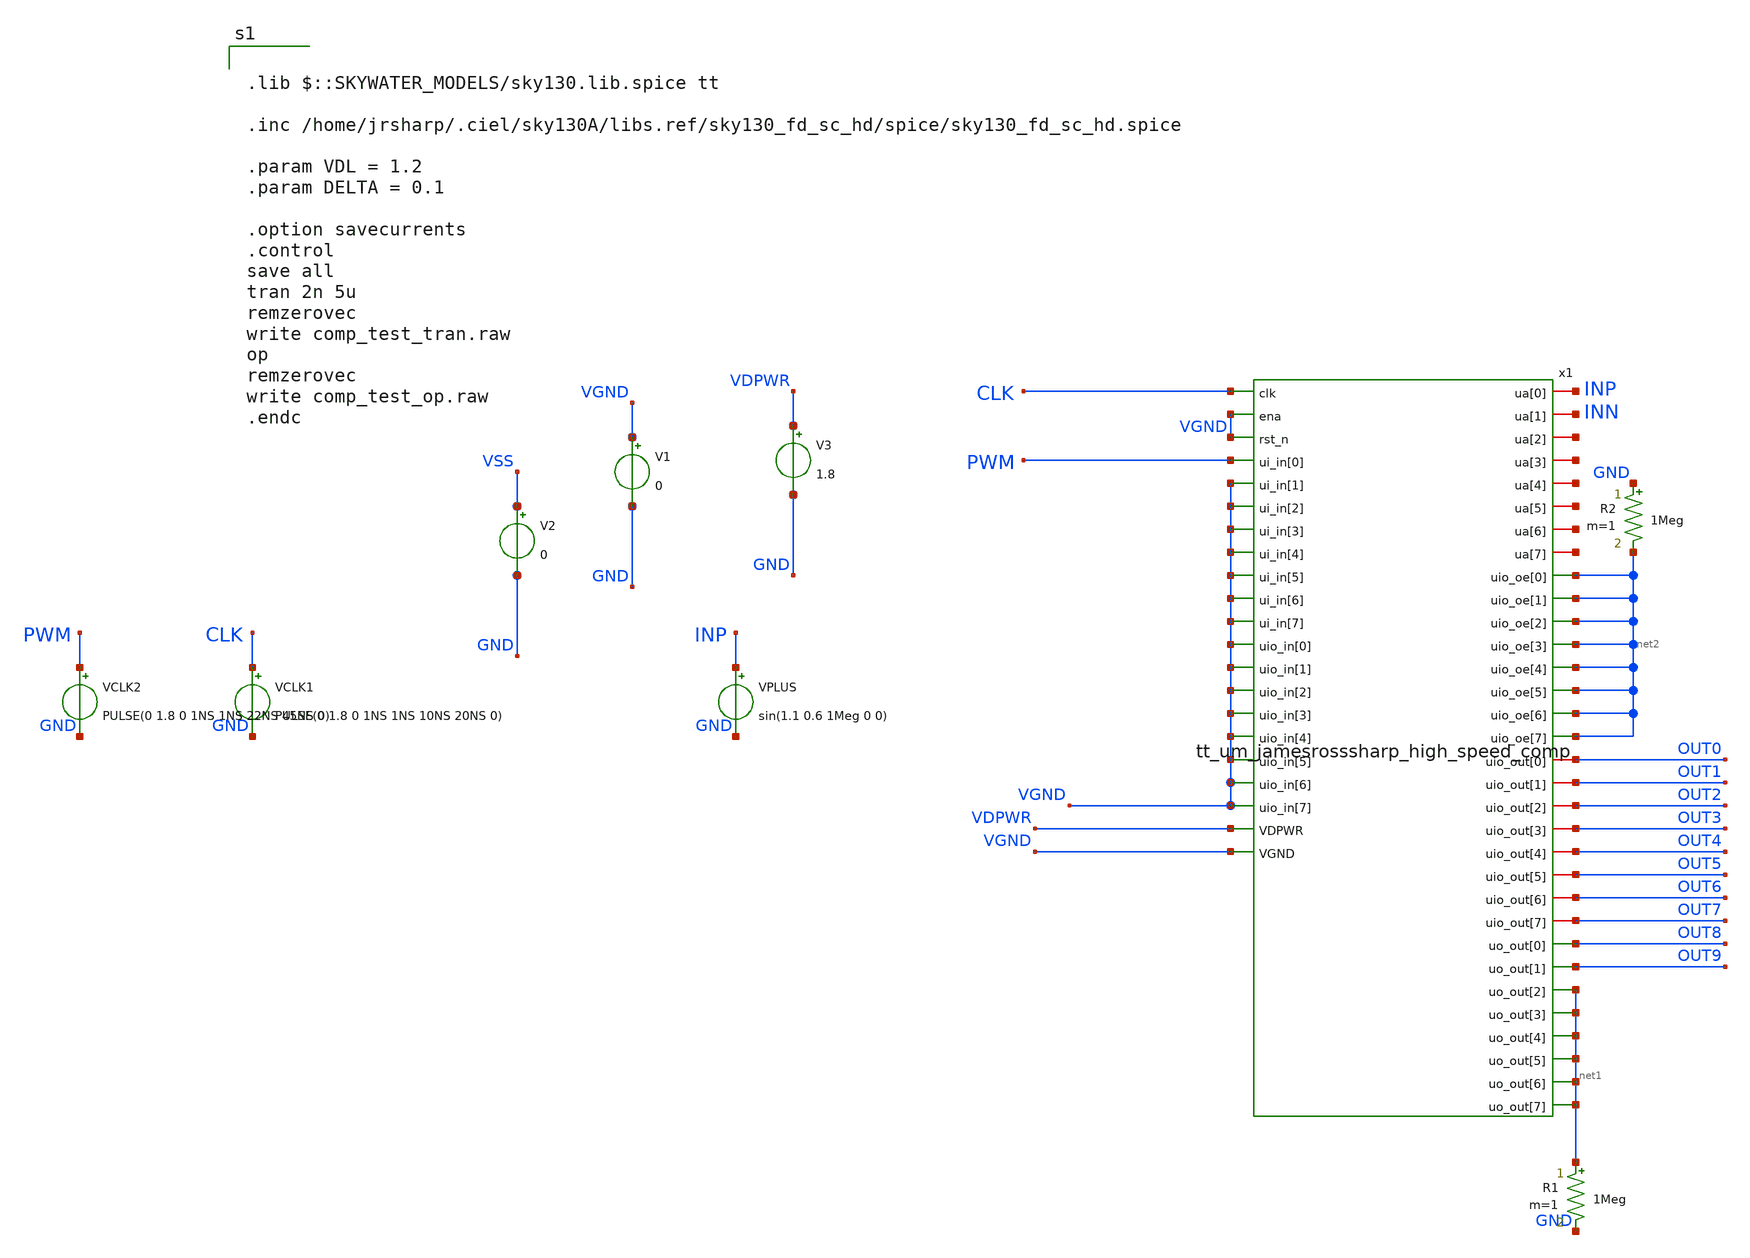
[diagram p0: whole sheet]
** sch_path: xschem/tt/tt_um_jamesrosssharp_high_speed_comp_test.sch
**.subckt tt_um_jamesrosssharp_high_speed_comp_test
x1 CLK VGND VGND PWM INP VGND INN VGND net3 VGND net4 VGND net5 VGND net6 VGND net7 VGND net8 VGND
+ VGND VGND VGND VGND VGND VGND VGND net2 net2 net2 net2 net2 net2 net2 net2 OUT0 OUT1 OUT2 OUT3 OUT4 OUT5
+ OUT6 OUT7 OUT8 OUT9 net1 net1 net1 net1 net1 net1 VDPWR VGND tt_um_jamesrosssharp_high_speed_comp
VPLUS INP GND sin(1.1 0.6 1Meg 0 0)
VCLK1 CLK GND PULSE(0 1.8 0 1NS 1NS 10NS 20NS 0)
V3 VDPWR GND 1.8
V1 VGND GND 0
R1 net1 GND 1Meg m=1
R2 GND net2 1Meg m=1
V2 VSS GND 0
VCLK2 PWM GND PULSE(0 1.8 0 1NS 1NS 22NS 45NS 0)
**** begin user architecture code

.lib $::SKYWATER_MODELS/sky130.lib.spice tt

.inc /home/jrsharp/.ciel/sky130A/libs.ref/sky130_fd_sc_hd/spice/sky130_fd_sc_hd.spice

.param VDL = 1.2
.param DELTA = 0.1

.option savecurrents
.control
save all
tran 2n 5u
remzerovec
write comp_test_tran.raw
op
remzerovec
write comp_test_op.raw
.endc



**** end user architecture code
**.ends

* expanding   symbol:  tt_um_jamesrosssharp_high_speed_comp.sym # of pins=53
** sym_path: xschem/tt/tt_um_jamesrosssharp_high_speed_comp.sym
** sch_path: xschem/tt/tt_um_jamesrosssharp_high_speed_comp.sch
.subckt tt_um_jamesrosssharp_high_speed_comp clk ena rst_n ui_in[0] ua[0] ui_in[1] ua[1] ui_in[2]
+ ua[2] ui_in[3] ua[3] ui_in[4] ua[4] ui_in[5] ua[5] ui_in[6] ua[6] ui_in[7] ua[7] uio_in[0] uio_in[1]
+ uio_in[2] uio_in[3] uio_in[4] uio_in[5] uio_in[6] uio_in[7] uio_oe[0] uio_oe[1] uio_oe[2] uio_oe[3] uio_oe[4]
+ uio_oe[5] uio_oe[6] uio_oe[7] uio_out[0] uio_out[1] uio_out[2] uio_out[3] uio_out[4] uio_out[5] uio_out[6]
+ uio_out[7] uo_out[0] uo_out[1] uo_out[2] uo_out[3] uo_out[4] uo_out[5] uo_out[6] uo_out[7] VDPWR VGND
*.ipin clk
*.ipin ena
*.ipin rst_n
*.iopin ua[0]
*.iopin ua[1]
*.iopin ua[2]
*.iopin ua[3]
*.iopin ua[4]
*.iopin ua[5]
*.iopin ua[6]
*.iopin ua[7]
*.ipin ui_in[0]
*.ipin ui_in[1]
*.ipin ui_in[2]
*.ipin ui_in[3]
*.ipin ui_in[4]
*.ipin ui_in[5]
*.ipin ui_in[6]
*.ipin ui_in[7]
*.ipin uio_in[0]
*.ipin uio_in[1]
*.ipin uio_in[2]
*.ipin uio_in[3]
*.ipin uio_in[4]
*.ipin uio_in[5]
*.ipin uio_in[6]
*.ipin uio_in[7]
*.opin uio_oe[0]
*.opin uio_oe[1]
*.opin uio_oe[2]
*.opin uio_oe[3]
*.opin uio_oe[4]
*.opin uio_oe[5]
*.opin uio_oe[6]
*.opin uio_oe[7]
*.iopin uio_out[0]
*.iopin uio_out[1]
*.iopin uio_out[2]
*.iopin uio_out[3]
*.iopin uio_out[4]
*.iopin uio_out[5]
*.iopin uio_out[6]
*.iopin uio_out[7]
*.opin uo_out[0]
*.opin uo_out[1]
*.opin uo_out[2]
*.opin uo_out[3]
*.opin uo_out[4]
*.opin uo_out[5]
*.opin uo_out[6]
*.opin uo_out[7]
*.ipin VDPWR
*.ipin VGND
x1 ua[0] VDPWR VGND ui_in[0] clk_prime net1 ua[1] 1bit_am
x2 net6 clk_prime ua[0] net14 net7 VDPWR VGND net8 net9 net13 net12 net11 net10 net3 flash_converter
x3 VGND VNB VPB VPWR uio_oe[0] net15 sky130_fd_sc_hd__conb_1
x4 VGND VNB VPB VPWR uio_oe[1] net16 sky130_fd_sc_hd__conb_1
x5 VGND VNB VPB VPWR uio_oe[2] net17 sky130_fd_sc_hd__conb_1
x6 VGND VNB VPB VPWR uio_oe[3] net18 sky130_fd_sc_hd__conb_1
x7 VGND VNB VPB VPWR uio_oe[4] net19 sky130_fd_sc_hd__conb_1
x8 VGND VNB VPB VPWR uio_oe[5] net20 sky130_fd_sc_hd__conb_1
x9 VGND VNB VPB VPWR uio_oe[6] net21 sky130_fd_sc_hd__conb_1
x10 VGND VNB VPB VPWR uio_oe[7] net22 sky130_fd_sc_hd__conb_1
x11 clk_prime ua[0] ua[1] VDPWR net2 VGND high_speed_comp_top
x12 VGND VNB VPB VPWR net23 uo_out[2] sky130_fd_sc_hd__conb_1
x13 VGND VNB VPB VPWR net24 uo_out[3] sky130_fd_sc_hd__conb_1
x14 VGND VNB VPB VPWR net25 uo_out[4] sky130_fd_sc_hd__conb_1
x15 VGND VNB VPB VPWR net26 uo_out[5] sky130_fd_sc_hd__conb_1
x16 VGND VNB VPB VPWR net27 uo_out[6] sky130_fd_sc_hd__conb_1
x17 VGND VNB VPB VPWR net28 uo_out[7] sky130_fd_sc_hd__conb_1
XR11 net6 VDPWR VGND sky130_fd_pr__res_high_po_1p41 L=1.41 mult=1 m=1
XR1 net3 net4 VGND sky130_fd_pr__res_high_po_1p41 L=1.41 mult=1 m=1
XR2 net4 net5 VGND sky130_fd_pr__res_high_po_1p41 L=1.41 mult=1 m=1
XR3 net5 VGND VGND sky130_fd_pr__res_high_po_1p41 L=1.41 mult=1 m=1
x18 clk VGND VGND VDPWR VDPWR clk_prime sky130_fd_sc_hd__clkbuf_16
x19 VGND VGND VDPWR VDPWR sky130_fd_sc_hd__decap_3
x20 VGND VDPWR sky130_fd_sc_hd__tapvpwrvgnd_1
x21 net2 VGND VGND VDPWR VDPWR uo_out[1] sky130_fd_sc_hd__buf_16
x22 net1 VGND VGND VDPWR VDPWR uo_out[0] sky130_fd_sc_hd__buf_16
x23 VGND VGND VDPWR VDPWR sky130_fd_sc_hd__decap_3
x24 VGND VDPWR sky130_fd_sc_hd__tapvpwrvgnd_1
x25 VGND VGND VDPWR VDPWR sky130_fd_sc_hd__decap_3
x26 VGND VDPWR sky130_fd_sc_hd__tapvpwrvgnd_1
x27 net14 VGND VGND VDPWR VDPWR uio_out[0] sky130_fd_sc_hd__buf_16
x28 net7 VGND VGND VDPWR VDPWR uio_out[1] sky130_fd_sc_hd__buf_16
x29 net8 VGND VGND VDPWR VDPWR uio_out[2] sky130_fd_sc_hd__buf_16
x31 net13 VGND VGND VDPWR VDPWR uio_out[4] sky130_fd_sc_hd__buf_16
x32 net12 VGND VGND VDPWR VDPWR uio_out[5] sky130_fd_sc_hd__buf_16
x33 net11 VGND VGND VDPWR VDPWR uio_out[6] sky130_fd_sc_hd__buf_16
x34 net10 VGND VGND VDPWR VDPWR uio_out[7] sky130_fd_sc_hd__buf_16
x30 net9 VGND VGND VDPWR VDPWR uio_out[3] sky130_fd_sc_hd__buf_16
x35 VGND VGND VDPWR VDPWR sky130_fd_sc_hd__decap_3
x36 VGND VDPWR sky130_fd_sc_hd__tapvpwrvgnd_1
x37 VGND VGND VDPWR VDPWR sky130_fd_sc_hd__decap_3
x38 VGND VDPWR sky130_fd_sc_hd__tapvpwrvgnd_1
x39 VGND VGND VDPWR VDPWR sky130_fd_sc_hd__decap_3
x40 VGND VDPWR sky130_fd_sc_hd__tapvpwrvgnd_1
.ends


* expanding   symbol:  1bit_am.sym # of pins=7
** sym_path: xschem/1bit_am/1bit_am.sym
** sch_path: xschem/1bit_am/1bit_am.sch
.subckt 1bit_am VIN VDD VSS PWM_IN CLK VOUT VIN_MINUS
*.ipin VDD
*.ipin VSS
*.ipin CLK
*.ipin VIN
*.opin VOUT
*.ipin PWM_IN
*.ipin VIN_MINUS
x1 CLK NET_IN VIN_MINUS VDD VOUT VSS high_speed_comp_top
XR2 net2 VIN_MINUS VSS sky130_fd_pr__res_xhigh_po_0p35 L=30 mult=1 m=1
XR3 VDD net3 VSS sky130_fd_pr__res_xhigh_po_0p35 L=20 mult=1 m=1
XR4 net3 NET_IN VSS sky130_fd_pr__res_xhigh_po_0p35 L=20 mult=1 m=1
XR5 NET_IN net4 VSS sky130_fd_pr__res_xhigh_po_0p35 L=20 mult=1 m=1
XR6 net4 VSS VSS sky130_fd_pr__res_xhigh_po_0p35 L=20 mult=1 m=1
XC1 VIN NET_IN sky130_fd_pr__cap_mim_m3_1 W=10 L=10 MF=20 m=20
XC2 VIN_MINUS VSS sky130_fd_pr__cap_mim_m3_1 W=10 L=10 MF=20 m=20
x4 VSS VSS VDD VDD sky130_fd_sc_hd__decap_3
x5 VSS VSS VDD VDD sky130_fd_sc_hd__decap_3
x6 VSS VDD sky130_fd_sc_hd__tapvpwrvgnd_1
x7 VSS VDD sky130_fd_sc_hd__tapvpwrvgnd_1
XR1 net5 net6 VSS sky130_fd_pr__res_xhigh_po_0p35 L=30 mult=1 m=1
x3 PWM_IN VSS VSS VDD VDD net1 sky130_fd_sc_hd__inv_1
XR7 net6 net7 VSS sky130_fd_pr__res_xhigh_po_0p35 L=30 mult=1 m=1
XR8 net7 net2 VSS sky130_fd_pr__res_xhigh_po_0p35 L=30 mult=1 m=1
x2 net1 VSS VSS VDD VDD net5 sky130_fd_sc_hd__inv_1
.ends


* expanding   symbol:  flash_converter.sym # of pins=14
** sym_path: xschem/flash_converter/flash_converter.sym
** sch_path: xschem/flash_converter/flash_converter.sch
.subckt flash_converter RES_TOP CLK VIN O0 O1 VDD VSS O2 O3 O4 O5 O6 O7 RES_OUT
*.ipin VIN
*.ipin RES_TOP
*.opin RES_OUT
*.opin O0
*.opin O1
*.opin O2
*.opin O3
*.opin O4
*.opin O5
*.opin O6
*.opin O7
*.ipin CLK
*.ipin VDD
*.ipin VSS
x1 CLK VIN RES_TOP VDD O0 VSS high_speed_comp_top
x2 CLK VIN net1 VDD O1 VSS high_speed_comp_top
x3 CLK VIN net2 VDD O2 VSS high_speed_comp_top
x4 CLK VIN net3 VDD O3 VSS high_speed_comp_top
x5 CLK VIN net4 VDD O4 VSS high_speed_comp_top
x6 CLK VIN net5 VDD O5 VSS high_speed_comp_top
x7 CLK VIN net6 VDD O6 VSS high_speed_comp_top
x8 CLK VIN net7 VDD O7 VSS high_speed_comp_top
XR1 net1 RES_TOP VSS sky130_fd_pr__res_high_po_1p41 L=1.41 mult=1 m=1
XR2 net2 net1 VSS sky130_fd_pr__res_high_po_1p41 L=1.41 mult=1 m=1
XR3 net3 net2 VSS sky130_fd_pr__res_high_po_1p41 L=1.41 mult=1 m=1
XR4 net4 net3 VSS sky130_fd_pr__res_high_po_1p41 L=1.41 mult=1 m=1
XR5 net5 net4 VSS sky130_fd_pr__res_high_po_1p41 L=1.41 mult=1 m=1
XR6 net6 net5 VSS sky130_fd_pr__res_high_po_1p41 L=1.41 mult=1 m=1
XR7 net7 net6 VSS sky130_fd_pr__res_high_po_1p41 L=1.41 mult=1 m=1
XR8 RES_OUT net7 VSS sky130_fd_pr__res_high_po_1p41 L=1.41 mult=1 m=1
XR9 net8 net9 VSS sky130_fd_pr__res_high_po_1p41 L=1.41 mult=1 m=1
XR10 net10 net11 VSS sky130_fd_pr__res_high_po_1p41 L=1.41 mult=1 m=1
XR11 net12 net13 VSS sky130_fd_pr__res_high_po_1p41 L=1.41 mult=1 m=1
XR12 net14 net15 VSS sky130_fd_pr__res_high_po_1p41 L=1.41 mult=1 m=1
.ends


* expanding   symbol:  high_speed_comp_top.sym # of pins=6
** sym_path: xschem/flash_converter/high_speed_comp_top.sym
** sch_path: xschem/flash_converter/high_speed_comp_top.sch
.subckt high_speed_comp_top CLK VINP VINN VDD COMP_OUT VSS
*.ipin VINP
*.ipin VINN
*.ipin CLK
*.opin COMP_OUT
*.ipin VDD
*.ipin VSS
x1 VDD CLK_PRIME net1 net2 VSS VINP VINN strong_arm_latch
x2 VDD net1 net2 VOUT VSS post_amplifier
x3 CLK VOUT VSS VSS VDD VDD COMP_OUT sky130_fd_sc_hd__dfxtp_2
x4 CLK VSS VSS VDD VDD CLK_PRIME sky130_fd_sc_hd__clkinv_4
x5 VSS VSS VDD VDD sky130_fd_sc_hd__decap_3
x7 VSS VSS VDD VDD sky130_fd_sc_hd__decap_3
x9 VSS VDD sky130_fd_sc_hd__tapvpwrvgnd_1
x6 VSS VDD sky130_fd_sc_hd__tapvpwrvgnd_1
x8 VSS VDD sky130_fd_sc_hd__tapvpwrvgnd_1
.ends


* expanding   symbol:  strong_arm_latch.sym # of pins=7
** sym_path: xschem/flash_converter/strong_arm_latch.sym
** sch_path: xschem/flash_converter/strong_arm_latch.sch
.subckt strong_arm_latch VDD CLK VOUT_PLUS VOUT_MINUS VSS VINP VINN
*.ipin VSS
*.ipin VDD
*.ipin CLK
*.ipin VINP
*.ipin VINN
*.opin VOUT_MINUS
*.opin VOUT_PLUS
XM1 net2 VINP net1 VSS sky130_fd_pr__nfet_01v8_lvt L=1 W=5 nf=1 ad='int((nf+1)/2) * W/nf * 0.29' as='int((nf+2)/2) * W/nf * 0.29'
+ pd='2*int((nf+1)/2) * (W/nf + 0.29)' ps='2*int((nf+2)/2) * (W/nf + 0.29)' nrd='0.29 / W' nrs='0.29 / W'
+ sa=0 sb=0 sd=0 mult=1 m=1
XM2 net3 VINN net1 VSS sky130_fd_pr__nfet_01v8_lvt L=1 W=5 nf=1 ad='int((nf+1)/2) * W/nf * 0.29' as='int((nf+2)/2) * W/nf * 0.29'
+ pd='2*int((nf+1)/2) * (W/nf + 0.29)' ps='2*int((nf+2)/2) * (W/nf + 0.29)' nrd='0.29 / W' nrs='0.29 / W'
+ sa=0 sb=0 sd=0 mult=1 m=1
XM3 net1 CLK VSS VSS sky130_fd_pr__nfet_01v8_lvt L=1 W=5 nf=1 ad='int((nf+1)/2) * W/nf * 0.29' as='int((nf+2)/2) * W/nf * 0.29'
+ pd='2*int((nf+1)/2) * (W/nf + 0.29)' ps='2*int((nf+2)/2) * (W/nf + 0.29)' nrd='0.29 / W' nrs='0.29 / W'
+ sa=0 sb=0 sd=0 mult=1 m=1
XM4 VOUT_PLUS VOUT_MINUS net2 VSS sky130_fd_pr__nfet_01v8 L=0.15 W=1 nf=1 ad='int((nf+1)/2) * W/nf * 0.29'
+ as='int((nf+2)/2) * W/nf * 0.29' pd='2*int((nf+1)/2) * (W/nf + 0.29)' ps='2*int((nf+2)/2) * (W/nf + 0.29)'
+ nrd='0.29 / W' nrs='0.29 / W' sa=0 sb=0 sd=0 mult=1 m=1
XM5 VOUT_MINUS VOUT_PLUS net3 VSS sky130_fd_pr__nfet_01v8 L=0.15 W=1 nf=1 ad='int((nf+1)/2) * W/nf * 0.29'
+ as='int((nf+2)/2) * W/nf * 0.29' pd='2*int((nf+1)/2) * (W/nf + 0.29)' ps='2*int((nf+2)/2) * (W/nf + 0.29)'
+ nrd='0.29 / W' nrs='0.29 / W' sa=0 sb=0 sd=0 mult=1 m=1
XM6 VOUT_PLUS VOUT_MINUS VDD VDD sky130_fd_pr__pfet_01v8 L=0.15 W=1 nf=1 ad='int((nf+1)/2) * W/nf * 0.29'
+ as='int((nf+2)/2) * W/nf * 0.29' pd='2*int((nf+1)/2) * (W/nf + 0.29)' ps='2*int((nf+2)/2) * (W/nf + 0.29)'
+ nrd='0.29 / W' nrs='0.29 / W' sa=0 sb=0 sd=0 mult=1 m=1
XM7 VOUT_MINUS VOUT_PLUS VDD VDD sky130_fd_pr__pfet_01v8 L=0.15 W=1 nf=1 ad='int((nf+1)/2) * W/nf * 0.29'
+ as='int((nf+2)/2) * W/nf * 0.29' pd='2*int((nf+1)/2) * (W/nf + 0.29)' ps='2*int((nf+2)/2) * (W/nf + 0.29)'
+ nrd='0.29 / W' nrs='0.29 / W' sa=0 sb=0 sd=0 mult=1 m=1
XM8 VOUT_PLUS CLK VDD VDD sky130_fd_pr__pfet_01v8 L=0.15 W=10 nf=1 ad='int((nf+1)/2) * W/nf * 0.29' as='int((nf+2)/2) * W/nf * 0.29'
+ pd='2*int((nf+1)/2) * (W/nf + 0.29)' ps='2*int((nf+2)/2) * (W/nf + 0.29)' nrd='0.29 / W' nrs='0.29 / W'
+ sa=0 sb=0 sd=0 mult=1 m=1
XM9 net2 CLK VDD VDD sky130_fd_pr__pfet_01v8 L=0.15 W=10 nf=1 ad='int((nf+1)/2) * W/nf * 0.29' as='int((nf+2)/2) * W/nf * 0.29'
+ pd='2*int((nf+1)/2) * (W/nf + 0.29)' ps='2*int((nf+2)/2) * (W/nf + 0.29)' nrd='0.29 / W' nrs='0.29 / W'
+ sa=0 sb=0 sd=0 mult=1 m=1
XM10 VOUT_MINUS CLK VDD VDD sky130_fd_pr__pfet_01v8 L=0.15 W=10 nf=1 ad='int((nf+1)/2) * W/nf * 0.29'
+ as='int((nf+2)/2) * W/nf * 0.29' pd='2*int((nf+1)/2) * (W/nf + 0.29)' ps='2*int((nf+2)/2) * (W/nf + 0.29)'
+ nrd='0.29 / W' nrs='0.29 / W' sa=0 sb=0 sd=0 mult=1 m=1
XM11 net3 CLK VDD VDD sky130_fd_pr__pfet_01v8 L=0.15 W=10 nf=1 ad='int((nf+1)/2) * W/nf * 0.29' as='int((nf+2)/2) * W/nf * 0.29'
+ pd='2*int((nf+1)/2) * (W/nf + 0.29)' ps='2*int((nf+2)/2) * (W/nf + 0.29)' nrd='0.29 / W' nrs='0.29 / W'
+ sa=0 sb=0 sd=0 mult=1 m=1
.ends


* expanding   symbol:  post_amplifier.sym # of pins=5
** sym_path: xschem/flash_converter/post_amplifier.sym
** sch_path: xschem/flash_converter/post_amplifier.sch
.subckt post_amplifier VDD VLAT_PLUS VLAT_MINUS VOUT VSS
*.ipin VLAT_PLUS
*.ipin VLAT_MINUS
*.ipin VDD
*.ipin VSS
*.opin VOUT
XM1 net1 VLAT_PLUS net4 VSS sky130_fd_pr__nfet_01v8 L=0.15 W=1 nf=1 ad='int((nf+1)/2) * W/nf * 0.29'
+ as='int((nf+2)/2) * W/nf * 0.29' pd='2*int((nf+1)/2) * (W/nf + 0.29)' ps='2*int((nf+2)/2) * (W/nf + 0.29)'
+ nrd='0.29 / W' nrs='0.29 / W' sa=0 sb=0 sd=0 mult=1 m=1
XM2 net3 VLAT_MINUS net4 VSS sky130_fd_pr__nfet_01v8 L=0.15 W=1 nf=1 ad='int((nf+1)/2) * W/nf * 0.29'
+ as='int((nf+2)/2) * W/nf * 0.29' pd='2*int((nf+1)/2) * (W/nf + 0.29)' ps='2*int((nf+2)/2) * (W/nf + 0.29)'
+ nrd='0.29 / W' nrs='0.29 / W' sa=0 sb=0 sd=0 mult=1 m=1
XM3 net4 net1 VSS VSS sky130_fd_pr__nfet_01v8 L=0.15 W=1 nf=1 ad='int((nf+1)/2) * W/nf * 0.29' as='int((nf+2)/2) * W/nf * 0.29'
+ pd='2*int((nf+1)/2) * (W/nf + 0.29)' ps='2*int((nf+2)/2) * (W/nf + 0.29)' nrd='0.29 / W' nrs='0.29 / W'
+ sa=0 sb=0 sd=0 mult=1 m=1
XM4 net1 VLAT_PLUS net2 VDD sky130_fd_pr__pfet_01v8 L=0.15 W=1 nf=1 ad='int((nf+1)/2) * W/nf * 0.29'
+ as='int((nf+2)/2) * W/nf * 0.29' pd='2*int((nf+1)/2) * (W/nf + 0.29)' ps='2*int((nf+2)/2) * (W/nf + 0.29)'
+ nrd='0.29 / W' nrs='0.29 / W' sa=0 sb=0 sd=0 mult=1 m=1
XM5 net3 VLAT_MINUS net2 VDD sky130_fd_pr__pfet_01v8 L=0.15 W=1 nf=1 ad='int((nf+1)/2) * W/nf * 0.29'
+ as='int((nf+2)/2) * W/nf * 0.29' pd='2*int((nf+1)/2) * (W/nf + 0.29)' ps='2*int((nf+2)/2) * (W/nf + 0.29)'
+ nrd='0.29 / W' nrs='0.29 / W' sa=0 sb=0 sd=0 mult=1 m=1
XM6 net2 net1 VDD VDD sky130_fd_pr__pfet_01v8 L=0.15 W=1 nf=1 ad='int((nf+1)/2) * W/nf * 0.29' as='int((nf+2)/2) * W/nf * 0.29'
+ pd='2*int((nf+1)/2) * (W/nf + 0.29)' ps='2*int((nf+2)/2) * (W/nf + 0.29)' nrd='0.29 / W' nrs='0.29 / W'
+ sa=0 sb=0 sd=0 mult=1 m=1
XM7 VOUT net3 VSS VSS sky130_fd_pr__nfet_01v8 L=0.15 W=1 nf=1 ad='int((nf+1)/2) * W/nf * 0.29' as='int((nf+2)/2) * W/nf * 0.29'
+ pd='2*int((nf+1)/2) * (W/nf + 0.29)' ps='2*int((nf+2)/2) * (W/nf + 0.29)' nrd='0.29 / W' nrs='0.29 / W'
+ sa=0 sb=0 sd=0 mult=1 m=1
XM8 VOUT net3 VDD VDD sky130_fd_pr__pfet_01v8 L=0.15 W=1 nf=1 ad='int((nf+1)/2) * W/nf * 0.29' as='int((nf+2)/2) * W/nf * 0.29'
+ pd='2*int((nf+1)/2) * (W/nf + 0.29)' ps='2*int((nf+2)/2) * (W/nf + 0.29)' nrd='0.29 / W' nrs='0.29 / W'
+ sa=0 sb=0 sd=0 mult=1 m=1
.ends

.GLOBAL VSS
.end
